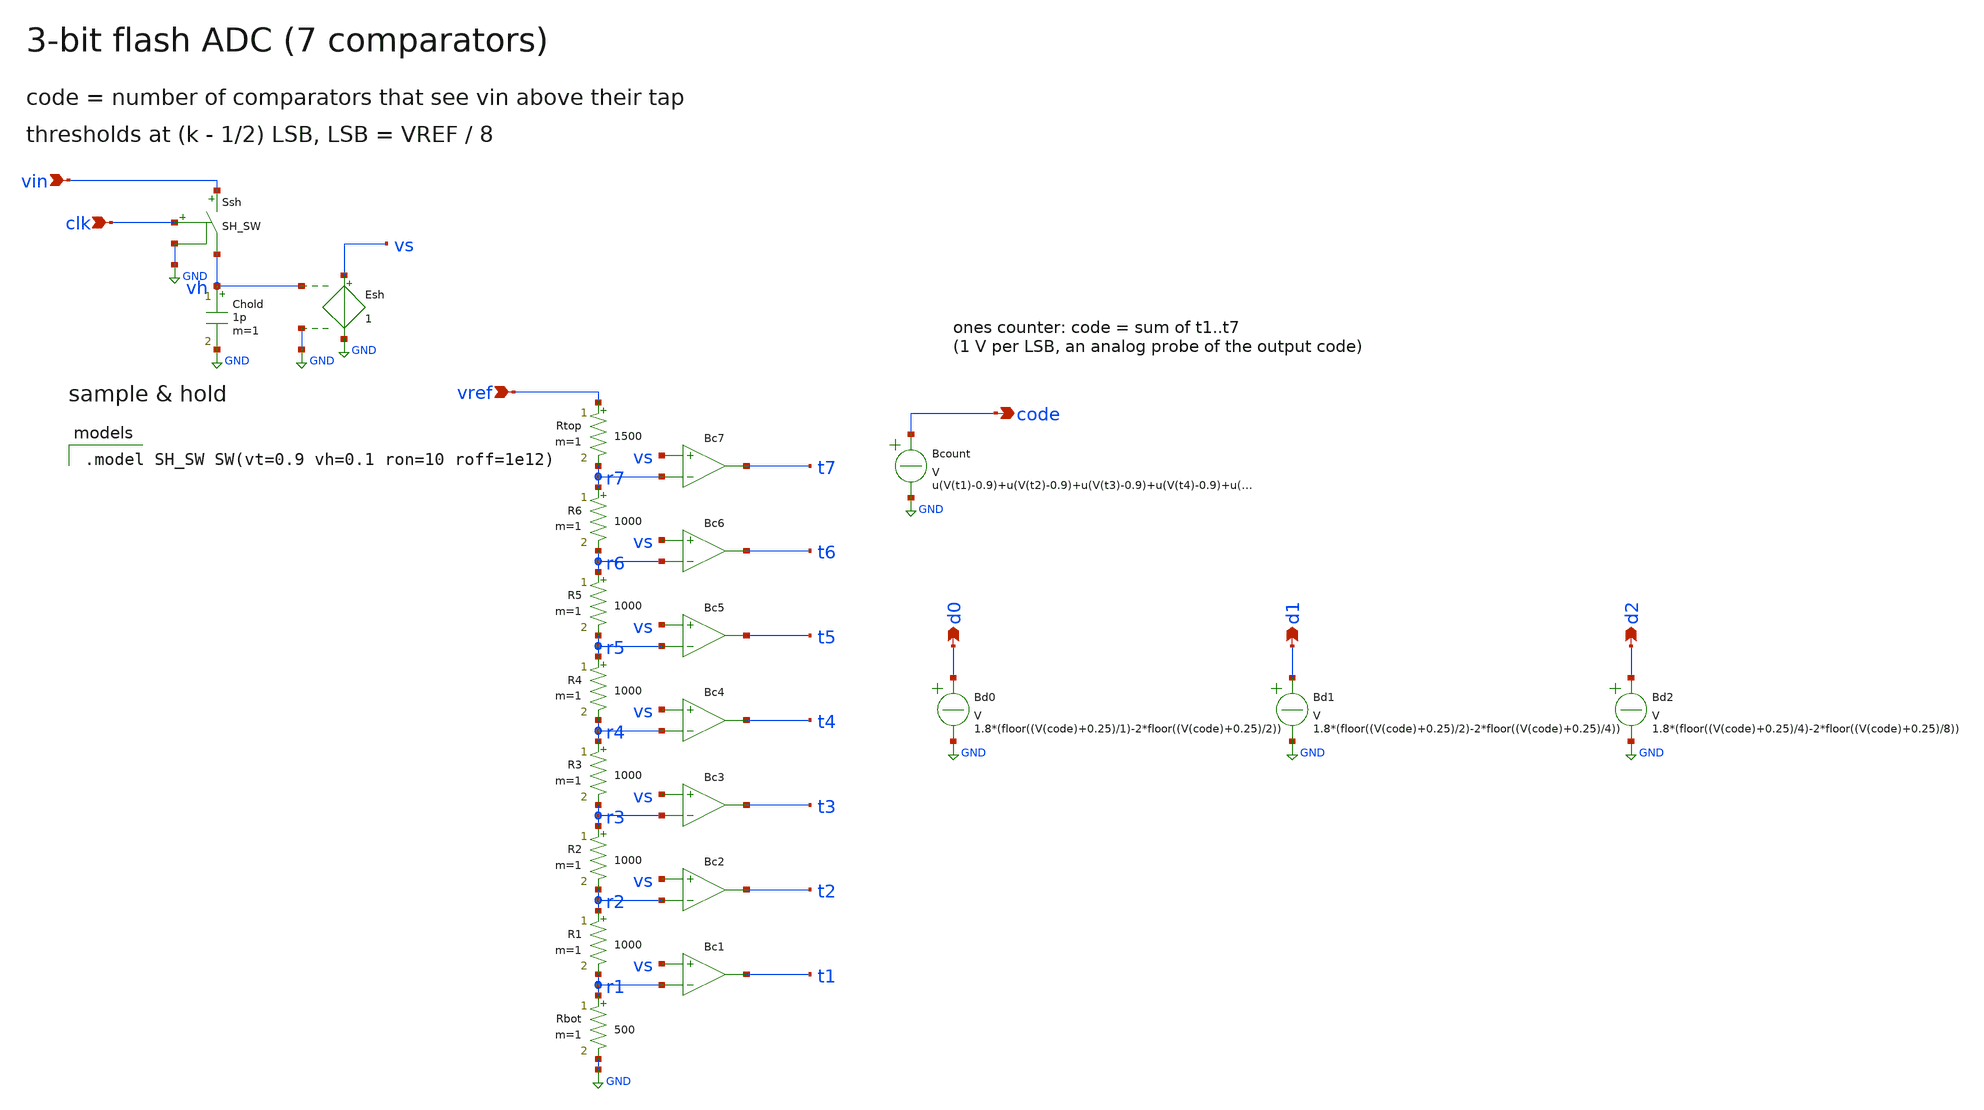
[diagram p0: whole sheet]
** sch_path: analog/sch/adc_flash3.sch
**.subckt adc_flash3 vin clk vref code d0 d1 d2
*.ipin vin
*.ipin clk
*.ipin vref
*.opin code
*.opin d0
*.opin d1
*.opin d2
Ssh vin vh clk GND SH_SW
Chold vh GND 1p m=1
Esh vs GND vh GND 1
Rtop vref r7 1500 m=1
R6 r7 r6 1000 m=1
R5 r6 r5 1000 m=1
R4 r5 r4 1000 m=1
R3 r4 r3 1000 m=1
R2 r3 r2 1000 m=1
R1 r2 r1 1000 m=1
Rbot r1 GND 500 m=1
Bc1 t1 0 V = 1.8 * (0.5 + 0.5 * tanh( 1e5 * (V( vs ) - V( r1 ))))
Bc2 t2 0 V = 1.8 * (0.5 + 0.5 * tanh( 1e5 * (V( vs ) - V( r2 ))))
Bc3 t3 0 V = 1.8 * (0.5 + 0.5 * tanh( 1e5 * (V( vs ) - V( r3 ))))
Bc4 t4 0 V = 1.8 * (0.5 + 0.5 * tanh( 1e5 * (V( vs ) - V( r4 ))))
Bc5 t5 0 V = 1.8 * (0.5 + 0.5 * tanh( 1e5 * (V( vs ) - V( r5 ))))
Bc6 t6 0 V = 1.8 * (0.5 + 0.5 * tanh( 1e5 * (V( vs ) - V( r6 ))))
Bc7 t7 0 V = 1.8 * (0.5 + 0.5 * tanh( 1e5 * (V( vs ) - V( r7 ))))
Bcount code GND V =
+ u(V(t1)-0.9)+u(V(t2)-0.9)+u(V(t3)-0.9)+u(V(t4)-0.9)+u(V(t5)-0.9)+u(V(t6)-0.9)+u(V(t7)-0.9)
Bd0 d0 GND V = 1.8*(floor((V(code)+0.25)/1)-2*floor((V(code)+0.25)/2))
Bd1 d1 GND V = 1.8*(floor((V(code)+0.25)/2)-2*floor((V(code)+0.25)/4))
Bd2 d2 GND V = 1.8*(floor((V(code)+0.25)/4)-2*floor((V(code)+0.25)/8))
**** begin user architecture code

.model SH_SW SW(vt=0.9 vh=0.1 ron=10 roff=1e12)

**** end user architecture code
**.ends
.GLOBAL GND
.end
